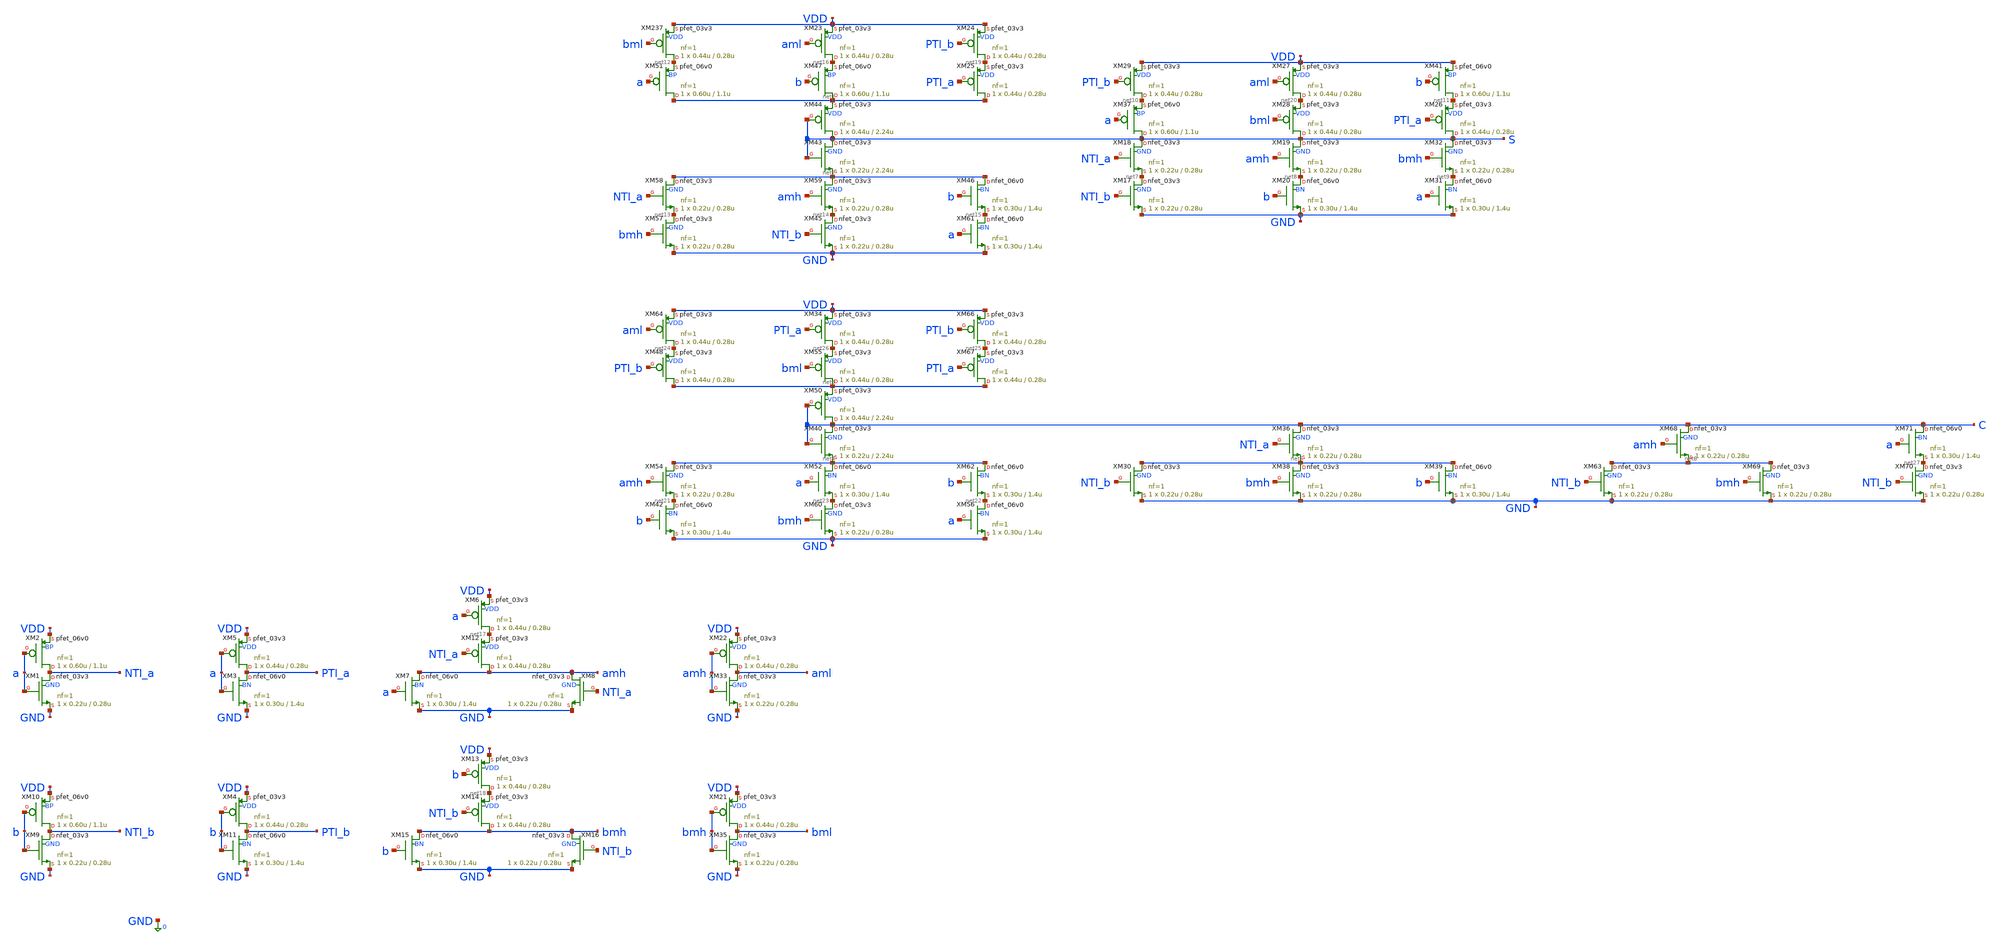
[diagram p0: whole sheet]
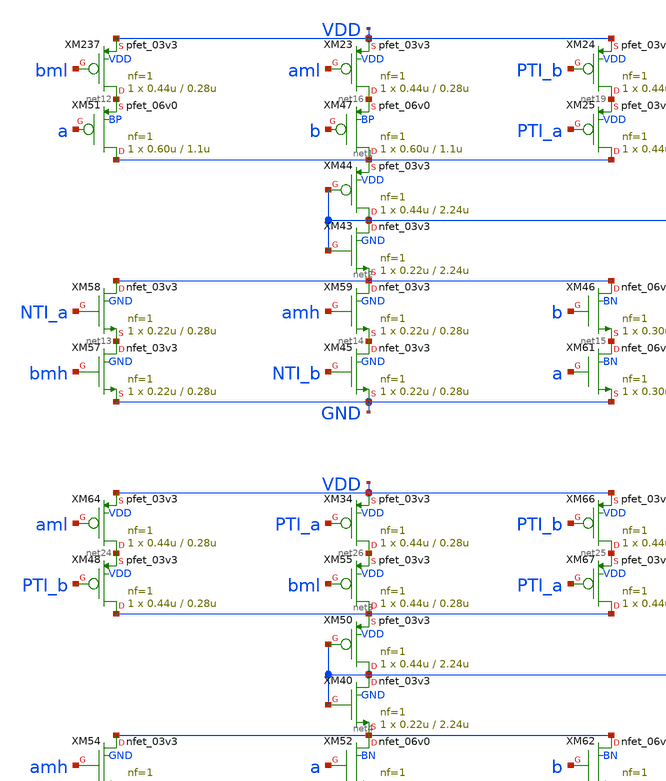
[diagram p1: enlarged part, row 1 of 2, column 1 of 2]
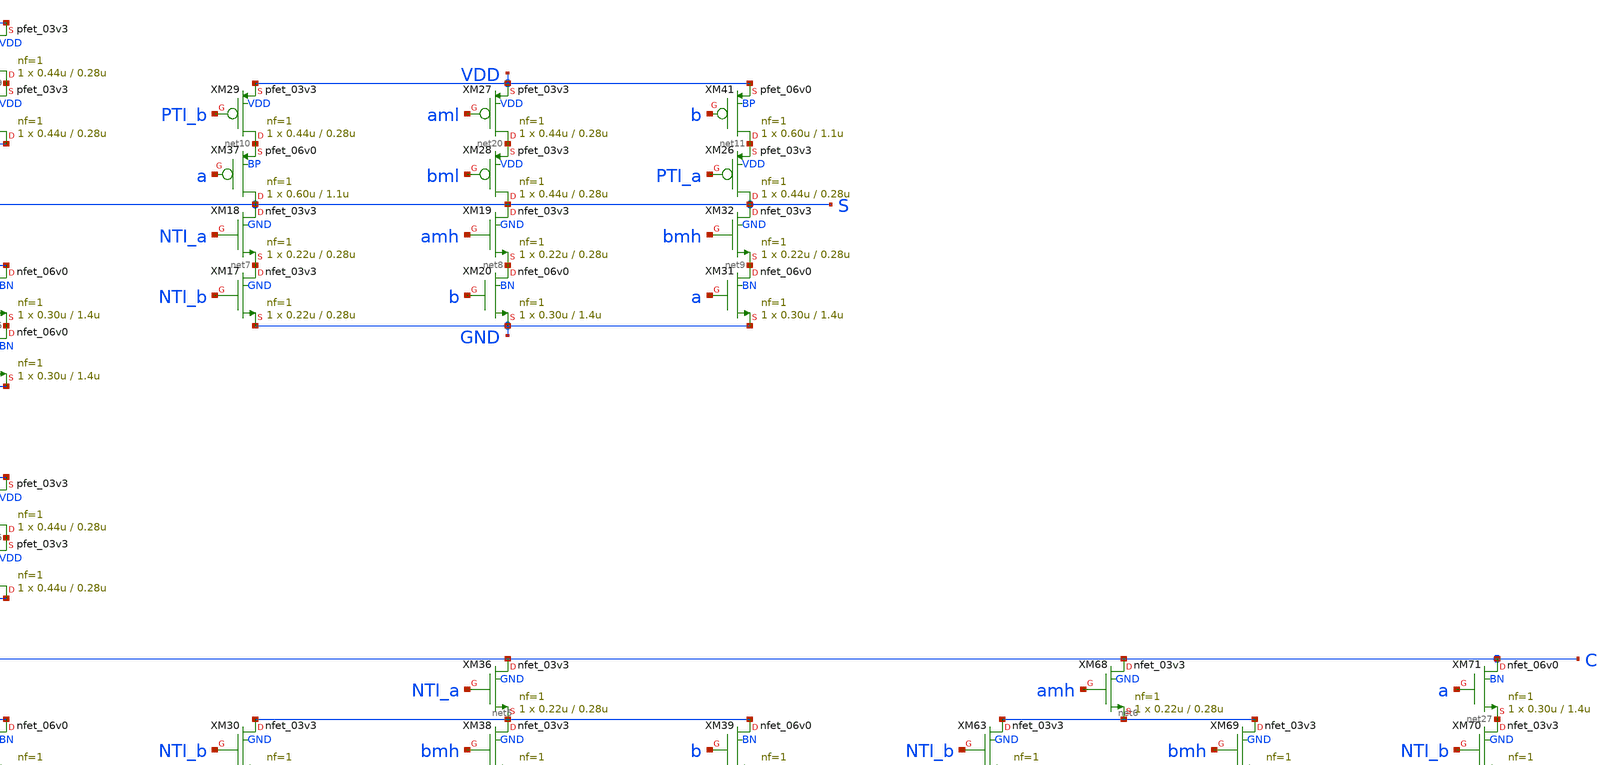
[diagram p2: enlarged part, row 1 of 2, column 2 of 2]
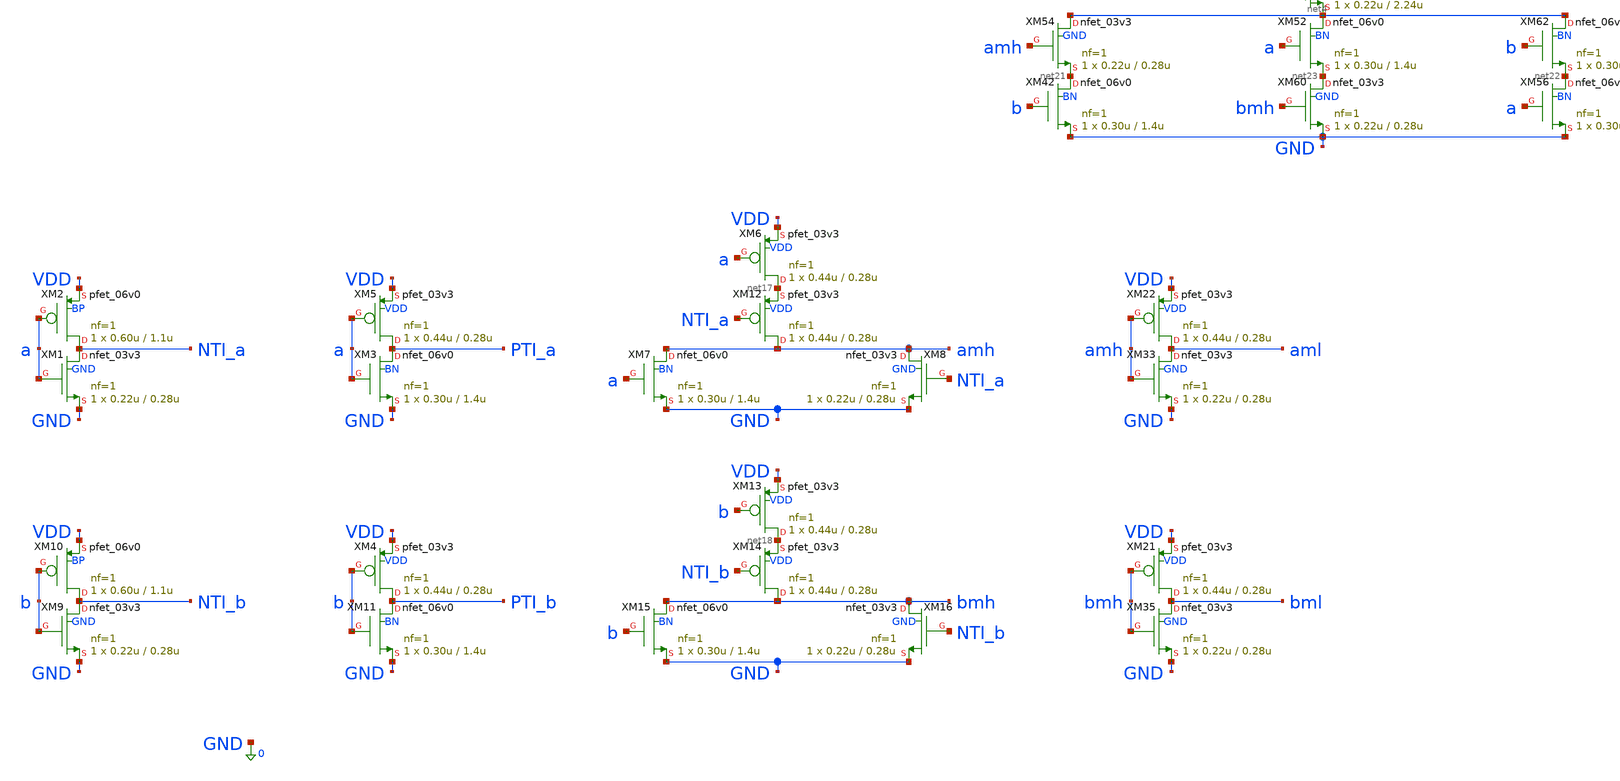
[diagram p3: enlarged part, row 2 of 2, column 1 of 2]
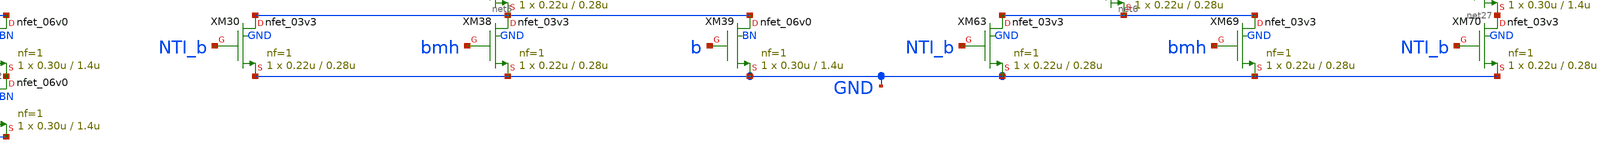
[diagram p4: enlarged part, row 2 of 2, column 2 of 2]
** sch_path: xschem_designs/SUM_TB.sch
**.subckt SUM_TB
XM1 NTI_a a GND GND nfet_03v3 L=0.28u W=0.22u nf=1 ad='int((nf+1)/2) * W/nf * 0.18u' as='int((nf+2)/2) * W/nf * 0.18u'
+ pd='2*int((nf+1)/2) * (W/nf + 0.18u)' ps='2*int((nf+2)/2) * (W/nf + 0.18u)' nrd='0.18u / W' nrs='0.18u / W'
+ sa=0 sb=0 sd=0 m=1 par=1
XM2 NTI_a a VDD BP pfet_06v0 L=1.1u W=0.60u nf=1 ad='int((nf+1)/2) * W/nf * 0.18u' as='int((nf+2)/2) * W/nf * 0.18u'
+ pd='2*int((nf+1)/2) * (W/nf + 0.18u)' ps='2*int((nf+2)/2) * (W/nf + 0.18u)' nrd='0.18u / W' nrs='0.18u / W'
+ sa=0 sb=0 sd=0 m=1 par=1
XM3 PTI_a a GND BN nfet_06v0 L=1.4u W=0.30u nf=1 ad='int((nf+1)/2) * W/nf * 0.18u' as='int((nf+2)/2) * W/nf * 0.18u'
+ pd='2*int((nf+1)/2) * (W/nf + 0.18u)' ps='2*int((nf+2)/2) * (W/nf + 0.18u)' nrd='0.18u / W' nrs='0.18u / W'
+ sa=0 sb=0 sd=0 m=1 par=1
XM7 amh a GND BN nfet_06v0 L=1.4u W=0.30u nf=1 ad='int((nf+1)/2) * W/nf * 0.18u' as='int((nf+2)/2) * W/nf * 0.18u'
+ pd='2*int((nf+1)/2) * (W/nf + 0.18u)' ps='2*int((nf+2)/2) * (W/nf + 0.18u)' nrd='0.18u / W' nrs='0.18u / W'
+ sa=0 sb=0 sd=0 m=1 par=1
XM8 amh NTI_a GND GND nfet_03v3 L=0.28u W=0.22u nf=1 ad='int((nf+1)/2) * W/nf * 0.18u' as='int((nf+2)/2) * W/nf * 0.18u'
+ pd='2*int((nf+1)/2) * (W/nf + 0.18u)' ps='2*int((nf+2)/2) * (W/nf + 0.18u)' nrd='0.18u / W' nrs='0.18u / W'
+ sa=0 sb=0 sd=0 m=1 par=1
XM9 NTI_b b GND GND nfet_03v3 L=0.28u W=0.22u nf=1 ad='int((nf+1)/2) * W/nf * 0.18u' as='int((nf+2)/2) * W/nf * 0.18u'
+ pd='2*int((nf+1)/2) * (W/nf + 0.18u)' ps='2*int((nf+2)/2) * (W/nf + 0.18u)' nrd='0.18u / W' nrs='0.18u / W'
+ sa=0 sb=0 sd=0 m=1 par=1
XM10 NTI_b b VDD BP pfet_06v0 L=1.1u W=0.60u nf=1 ad='int((nf+1)/2) * W/nf * 0.18u' as='int((nf+2)/2) * W/nf * 0.18u'
+ pd='2*int((nf+1)/2) * (W/nf + 0.18u)' ps='2*int((nf+2)/2) * (W/nf + 0.18u)' nrd='0.18u / W' nrs='0.18u / W'
+ sa=0 sb=0 sd=0 m=1 par=1
XM11 PTI_b b GND BN nfet_06v0 L=1.4u W=0.30u nf=1 ad='int((nf+1)/2) * W/nf * 0.18u' as='int((nf+2)/2) * W/nf * 0.18u'
+ pd='2*int((nf+1)/2) * (W/nf + 0.18u)' ps='2*int((nf+2)/2) * (W/nf + 0.18u)' nrd='0.18u / W' nrs='0.18u / W'
+ sa=0 sb=0 sd=0 m=1 par=1
XM15 bmh b GND BN nfet_06v0 L=1.4u W=0.30u nf=1 ad='int((nf+1)/2) * W/nf * 0.18u' as='int((nf+2)/2) * W/nf * 0.18u'
+ pd='2*int((nf+1)/2) * (W/nf + 0.18u)' ps='2*int((nf+2)/2) * (W/nf + 0.18u)' nrd='0.18u / W' nrs='0.18u / W'
+ sa=0 sb=0 sd=0 m=1 par=1
XM16 bmh NTI_b GND GND nfet_03v3 L=0.28u W=0.22u nf=1 ad='int((nf+1)/2) * W/nf * 0.18u' as='int((nf+2)/2) * W/nf * 0.18u'
+ pd='2*int((nf+1)/2) * (W/nf + 0.18u)' ps='2*int((nf+2)/2) * (W/nf + 0.18u)' nrd='0.18u / W' nrs='0.18u / W'
+ sa=0 sb=0 sd=0 m=1 par=1
XM17 net7 NTI_b GND GND nfet_03v3 L=0.28u W=0.22u nf=1 ad='int((nf+1)/2) * W/nf * 0.18u' as='int((nf+2)/2) * W/nf * 0.18u'
+ pd='2*int((nf+1)/2) * (W/nf + 0.18u)' ps='2*int((nf+2)/2) * (W/nf + 0.18u)' nrd='0.18u / W' nrs='0.18u / W'
+ sa=0 sb=0 sd=0 m=1 par=1
XM18 S NTI_a net7 GND nfet_03v3 L=0.28u W=0.22u nf=1 ad='int((nf+1)/2) * W/nf * 0.18u' as='int((nf+2)/2) * W/nf * 0.18u'
+ pd='2*int((nf+1)/2) * (W/nf + 0.18u)' ps='2*int((nf+2)/2) * (W/nf + 0.18u)' nrd='0.18u / W' nrs='0.18u / W'
+ sa=0 sb=0 sd=0 m=1 par=1
XM19 S amh net8 GND nfet_03v3 L=0.28u W=0.22u nf=1 ad='int((nf+1)/2) * W/nf * 0.18u' as='int((nf+2)/2) * W/nf * 0.18u'
+ pd='2*int((nf+1)/2) * (W/nf + 0.18u)' ps='2*int((nf+2)/2) * (W/nf + 0.18u)' nrd='0.18u / W' nrs='0.18u / W'
+ sa=0 sb=0 sd=0 m=1 par=1
XM20 net8 b GND BN nfet_06v0 L=1.4u W=0.30u nf=1 ad='int((nf+1)/2) * W/nf * 0.18u' as='int((nf+2)/2) * W/nf * 0.18u'
+ pd='2*int((nf+1)/2) * (W/nf + 0.18u)' ps='2*int((nf+2)/2) * (W/nf + 0.18u)' nrd='0.18u / W' nrs='0.18u / W'
+ sa=0 sb=0 sd=0 m=1 par=1
XM31 net9 a GND BN nfet_06v0 L=1.4u W=0.30u nf=1 ad='int((nf+1)/2) * W/nf * 0.18u' as='int((nf+2)/2) * W/nf * 0.18u'
+ pd='2*int((nf+1)/2) * (W/nf + 0.18u)' ps='2*int((nf+2)/2) * (W/nf + 0.18u)' nrd='0.18u / W' nrs='0.18u / W'
+ sa=0 sb=0 sd=0 m=1 par=1
XM32 S bmh net9 GND nfet_03v3 L=0.28u W=0.22u nf=1 ad='int((nf+1)/2) * W/nf * 0.18u' as='int((nf+2)/2) * W/nf * 0.18u'
+ pd='2*int((nf+1)/2) * (W/nf + 0.18u)' ps='2*int((nf+2)/2) * (W/nf + 0.18u)' nrd='0.18u / W' nrs='0.18u / W'
+ sa=0 sb=0 sd=0 m=1 par=1
XM33 aml amh GND GND nfet_03v3 L=0.28u W=0.22u nf=1 ad='int((nf+1)/2) * W/nf * 0.18u' as='int((nf+2)/2) * W/nf * 0.18u'
+ pd='2*int((nf+1)/2) * (W/nf + 0.18u)' ps='2*int((nf+2)/2) * (W/nf + 0.18u)' nrd='0.18u / W' nrs='0.18u / W'
+ sa=0 sb=0 sd=0 m=1 par=1
XM35 bml bmh GND GND nfet_03v3 L=0.28u W=0.22u nf=1 ad='int((nf+1)/2) * W/nf * 0.18u' as='int((nf+2)/2) * W/nf * 0.18u'
+ pd='2*int((nf+1)/2) * (W/nf + 0.18u)' ps='2*int((nf+2)/2) * (W/nf + 0.18u)' nrd='0.18u / W' nrs='0.18u / W'
+ sa=0 sb=0 sd=0 m=1 par=1
XM37 S a net10 BP pfet_06v0 L=1.1u W=0.60u nf=1 ad='int((nf+1)/2) * W/nf * 0.18u' as='int((nf+2)/2) * W/nf * 0.18u'
+ pd='2*int((nf+1)/2) * (W/nf + 0.18u)' ps='2*int((nf+2)/2) * (W/nf + 0.18u)' nrd='0.18u / W' nrs='0.18u / W'
+ sa=0 sb=0 sd=0 m=1 par=1
XM41 net11 b VDD BP pfet_06v0 L=1.1u W=0.60u nf=1 ad='int((nf+1)/2) * W/nf * 0.18u' as='int((nf+2)/2) * W/nf * 0.18u'
+ pd='2*int((nf+1)/2) * (W/nf + 0.18u)' ps='2*int((nf+2)/2) * (W/nf + 0.18u)' nrd='0.18u / W' nrs='0.18u / W'
+ sa=0 sb=0 sd=0 m=1 par=1
XM43 S S net2 GND nfet_03v3 L=2.24u W=0.22u nf=1 ad='int((nf+1)/2) * W/nf * 0.18u' as='int((nf+2)/2) * W/nf * 0.18u'
+ pd='2*int((nf+1)/2) * (W/nf + 0.18u)' ps='2*int((nf+2)/2) * (W/nf + 0.18u)' nrd='0.18u / W' nrs='0.18u / W'
+ sa=0 sb=0 sd=0 m=1 par=1
XM44 S S net1 VDD pfet_03v3 L=2.24u W=0.44u nf=1 ad='int((nf+1)/2) * W/nf * 0.18u' as='int((nf+2)/2) * W/nf * 0.18u'
+ pd='2*int((nf+1)/2) * (W/nf + 0.18u)' ps='2*int((nf+2)/2) * (W/nf + 0.18u)' nrd='0.18u / W' nrs='0.18u / W'
+ sa=0 sb=0 sd=0 m=1 par=1
XM51 net1 a net12 BP pfet_06v0 L=1.1u W=0.60u nf=1 ad='int((nf+1)/2) * W/nf * 0.18u' as='int((nf+2)/2) * W/nf * 0.18u'
+ pd='2*int((nf+1)/2) * (W/nf + 0.18u)' ps='2*int((nf+2)/2) * (W/nf + 0.18u)' nrd='0.18u / W' nrs='0.18u / W'
+ sa=0 sb=0 sd=0 m=1 par=1
XM57 net13 bmh GND GND nfet_03v3 L=0.28u W=0.22u nf=1 ad='int((nf+1)/2) * W/nf * 0.18u' as='int((nf+2)/2) * W/nf * 0.18u'
+ pd='2*int((nf+1)/2) * (W/nf + 0.18u)' ps='2*int((nf+2)/2) * (W/nf + 0.18u)' nrd='0.18u / W' nrs='0.18u / W'
+ sa=0 sb=0 sd=0 m=1 par=1
XM58 net2 NTI_a net13 GND nfet_03v3 L=0.28u W=0.22u nf=1 ad='int((nf+1)/2) * W/nf * 0.18u' as='int((nf+2)/2) * W/nf * 0.18u'
+ pd='2*int((nf+1)/2) * (W/nf + 0.18u)' ps='2*int((nf+2)/2) * (W/nf + 0.18u)' nrd='0.18u / W' nrs='0.18u / W'
+ sa=0 sb=0 sd=0 m=1 par=1
XM59 net2 amh net14 GND nfet_03v3 L=0.28u W=0.22u nf=1 ad='int((nf+1)/2) * W/nf * 0.18u' as='int((nf+2)/2) * W/nf * 0.18u'
+ pd='2*int((nf+1)/2) * (W/nf + 0.18u)' ps='2*int((nf+2)/2) * (W/nf + 0.18u)' nrd='0.18u / W' nrs='0.18u / W'
+ sa=0 sb=0 sd=0 m=1 par=1
XM61 net15 a GND BN nfet_06v0 L=1.4u W=0.30u nf=1 ad='int((nf+1)/2) * W/nf * 0.18u' as='int((nf+2)/2) * W/nf * 0.18u'
+ pd='2*int((nf+1)/2) * (W/nf + 0.18u)' ps='2*int((nf+2)/2) * (W/nf + 0.18u)' nrd='0.18u / W' nrs='0.18u / W'
+ sa=0 sb=0 sd=0 m=1 par=1
XM45 net14 NTI_b GND GND nfet_03v3 L=0.28u W=0.22u nf=1 ad='int((nf+1)/2) * W/nf * 0.18u' as='int((nf+2)/2) * W/nf * 0.18u'
+ pd='2*int((nf+1)/2) * (W/nf + 0.18u)' ps='2*int((nf+2)/2) * (W/nf + 0.18u)' nrd='0.18u / W' nrs='0.18u / W'
+ sa=0 sb=0 sd=0 m=1 par=1
XM46 net2 b net15 BN nfet_06v0 L=1.4u W=0.30u nf=1 ad='int((nf+1)/2) * W/nf * 0.18u' as='int((nf+2)/2) * W/nf * 0.18u'
+ pd='2*int((nf+1)/2) * (W/nf + 0.18u)' ps='2*int((nf+2)/2) * (W/nf + 0.18u)' nrd='0.18u / W' nrs='0.18u / W'
+ sa=0 sb=0 sd=0 m=1 par=1
XM47 net1 b net16 BP pfet_06v0 L=1.1u W=0.60u nf=1 ad='int((nf+1)/2) * W/nf * 0.18u' as='int((nf+2)/2) * W/nf * 0.18u'
+ pd='2*int((nf+1)/2) * (W/nf + 0.18u)' ps='2*int((nf+2)/2) * (W/nf + 0.18u)' nrd='0.18u / W' nrs='0.18u / W'
+ sa=0 sb=0 sd=0 m=1 par=1
XM237 net12 bml VDD VDD pfet_03v3 L=0.28u W=0.44u nf=1 ad='int((nf+1)/2) * W/nf * 0.18u' as='int((nf+2)/2) * W/nf * 0.18u'
+ pd='2*int((nf+1)/2) * (W/nf + 0.18u)' ps='2*int((nf+2)/2) * (W/nf + 0.18u)' nrd='0.18u / W' nrs='0.18u / W'
+ sa=0 sb=0 sd=0 m=1 par=1
XM4 PTI_b b VDD VDD pfet_03v3 L=0.28u W=0.44u nf=1 ad='int((nf+1)/2) * W/nf * 0.18u' as='int((nf+2)/2) * W/nf * 0.18u'
+ pd='2*int((nf+1)/2) * (W/nf + 0.18u)' ps='2*int((nf+2)/2) * (W/nf + 0.18u)' nrd='0.18u / W' nrs='0.18u / W'
+ sa=0 sb=0 sd=0 m=1 par=1
XM5 PTI_a a VDD VDD pfet_03v3 L=0.28u W=0.44u nf=1 ad='int((nf+1)/2) * W/nf * 0.18u' as='int((nf+2)/2) * W/nf * 0.18u'
+ pd='2*int((nf+1)/2) * (W/nf + 0.18u)' ps='2*int((nf+2)/2) * (W/nf + 0.18u)' nrd='0.18u / W' nrs='0.18u / W'
+ sa=0 sb=0 sd=0 m=1 par=1
XM6 net17 a VDD VDD pfet_03v3 L=0.28u W=0.44u nf=1 ad='int((nf+1)/2) * W/nf * 0.18u' as='int((nf+2)/2) * W/nf * 0.18u'
+ pd='2*int((nf+1)/2) * (W/nf + 0.18u)' ps='2*int((nf+2)/2) * (W/nf + 0.18u)' nrd='0.18u / W' nrs='0.18u / W'
+ sa=0 sb=0 sd=0 m=1 par=1
XM12 amh NTI_a net17 VDD pfet_03v3 L=0.28u W=0.44u nf=1 ad='int((nf+1)/2) * W/nf * 0.18u' as='int((nf+2)/2) * W/nf * 0.18u'
+ pd='2*int((nf+1)/2) * (W/nf + 0.18u)' ps='2*int((nf+2)/2) * (W/nf + 0.18u)' nrd='0.18u / W' nrs='0.18u / W'
+ sa=0 sb=0 sd=0 m=1 par=1
XM13 net18 b VDD VDD pfet_03v3 L=0.28u W=0.44u nf=1 ad='int((nf+1)/2) * W/nf * 0.18u' as='int((nf+2)/2) * W/nf * 0.18u'
+ pd='2*int((nf+1)/2) * (W/nf + 0.18u)' ps='2*int((nf+2)/2) * (W/nf + 0.18u)' nrd='0.18u / W' nrs='0.18u / W'
+ sa=0 sb=0 sd=0 m=1 par=1
XM14 bmh NTI_b net18 VDD pfet_03v3 L=0.28u W=0.44u nf=1 ad='int((nf+1)/2) * W/nf * 0.18u' as='int((nf+2)/2) * W/nf * 0.18u'
+ pd='2*int((nf+1)/2) * (W/nf + 0.18u)' ps='2*int((nf+2)/2) * (W/nf + 0.18u)' nrd='0.18u / W' nrs='0.18u / W'
+ sa=0 sb=0 sd=0 m=1 par=1
XM21 bml bmh VDD VDD pfet_03v3 L=0.28u W=0.44u nf=1 ad='int((nf+1)/2) * W/nf * 0.18u' as='int((nf+2)/2) * W/nf * 0.18u'
+ pd='2*int((nf+1)/2) * (W/nf + 0.18u)' ps='2*int((nf+2)/2) * (W/nf + 0.18u)' nrd='0.18u / W' nrs='0.18u / W'
+ sa=0 sb=0 sd=0 m=1 par=1
XM22 aml amh VDD VDD pfet_03v3 L=0.28u W=0.44u nf=1 ad='int((nf+1)/2) * W/nf * 0.18u' as='int((nf+2)/2) * W/nf * 0.18u'
+ pd='2*int((nf+1)/2) * (W/nf + 0.18u)' ps='2*int((nf+2)/2) * (W/nf + 0.18u)' nrd='0.18u / W' nrs='0.18u / W'
+ sa=0 sb=0 sd=0 m=1 par=1
XM23 net16 aml VDD VDD pfet_03v3 L=0.28u W=0.44u nf=1 ad='int((nf+1)/2) * W/nf * 0.18u' as='int((nf+2)/2) * W/nf * 0.18u'
+ pd='2*int((nf+1)/2) * (W/nf + 0.18u)' ps='2*int((nf+2)/2) * (W/nf + 0.18u)' nrd='0.18u / W' nrs='0.18u / W'
+ sa=0 sb=0 sd=0 m=1 par=1
XM24 net19 PTI_b VDD VDD pfet_03v3 L=0.28u W=0.44u nf=1 ad='int((nf+1)/2) * W/nf * 0.18u' as='int((nf+2)/2) * W/nf * 0.18u'
+ pd='2*int((nf+1)/2) * (W/nf + 0.18u)' ps='2*int((nf+2)/2) * (W/nf + 0.18u)' nrd='0.18u / W' nrs='0.18u / W'
+ sa=0 sb=0 sd=0 m=1 par=1
XM25 net1 PTI_a net19 VDD pfet_03v3 L=0.28u W=0.44u nf=1 ad='int((nf+1)/2) * W/nf * 0.18u' as='int((nf+2)/2) * W/nf * 0.18u'
+ pd='2*int((nf+1)/2) * (W/nf + 0.18u)' ps='2*int((nf+2)/2) * (W/nf + 0.18u)' nrd='0.18u / W' nrs='0.18u / W'
+ sa=0 sb=0 sd=0 m=1 par=1
XM26 S PTI_a net11 VDD pfet_03v3 L=0.28u W=0.44u nf=1 ad='int((nf+1)/2) * W/nf * 0.18u' as='int((nf+2)/2) * W/nf * 0.18u'
+ pd='2*int((nf+1)/2) * (W/nf + 0.18u)' ps='2*int((nf+2)/2) * (W/nf + 0.18u)' nrd='0.18u / W' nrs='0.18u / W'
+ sa=0 sb=0 sd=0 m=1 par=1
XM27 net20 aml VDD VDD pfet_03v3 L=0.28u W=0.44u nf=1 ad='int((nf+1)/2) * W/nf * 0.18u' as='int((nf+2)/2) * W/nf * 0.18u'
+ pd='2*int((nf+1)/2) * (W/nf + 0.18u)' ps='2*int((nf+2)/2) * (W/nf + 0.18u)' nrd='0.18u / W' nrs='0.18u / W'
+ sa=0 sb=0 sd=0 m=1 par=1
XM28 S bml net20 VDD pfet_03v3 L=0.28u W=0.44u nf=1 ad='int((nf+1)/2) * W/nf * 0.18u' as='int((nf+2)/2) * W/nf * 0.18u'
+ pd='2*int((nf+1)/2) * (W/nf + 0.18u)' ps='2*int((nf+2)/2) * (W/nf + 0.18u)' nrd='0.18u / W' nrs='0.18u / W'
+ sa=0 sb=0 sd=0 m=1 par=1
XM29 net10 PTI_b VDD VDD pfet_03v3 L=0.28u W=0.44u nf=1 ad='int((nf+1)/2) * W/nf * 0.18u' as='int((nf+2)/2) * W/nf * 0.18u'
+ pd='2*int((nf+1)/2) * (W/nf + 0.18u)' ps='2*int((nf+2)/2) * (W/nf + 0.18u)' nrd='0.18u / W' nrs='0.18u / W'
+ sa=0 sb=0 sd=0 m=1 par=1
XM30 net5 NTI_b GND GND nfet_03v3 L=0.28u W=0.22u nf=1 ad='int((nf+1)/2) * W/nf * 0.18u' as='int((nf+2)/2) * W/nf * 0.18u'
+ pd='2*int((nf+1)/2) * (W/nf + 0.18u)' ps='2*int((nf+2)/2) * (W/nf + 0.18u)' nrd='0.18u / W' nrs='0.18u / W'
+ sa=0 sb=0 sd=0 m=1 par=1
XM36 C NTI_a net5 GND nfet_03v3 L=0.28u W=0.22u nf=1 ad='int((nf+1)/2) * W/nf * 0.18u' as='int((nf+2)/2) * W/nf * 0.18u'
+ pd='2*int((nf+1)/2) * (W/nf + 0.18u)' ps='2*int((nf+2)/2) * (W/nf + 0.18u)' nrd='0.18u / W' nrs='0.18u / W'
+ sa=0 sb=0 sd=0 m=1 par=1
XM39 net5 b GND BN nfet_06v0 L=1.4u W=0.30u nf=1 ad='int((nf+1)/2) * W/nf * 0.18u' as='int((nf+2)/2) * W/nf * 0.18u'
+ pd='2*int((nf+1)/2) * (W/nf + 0.18u)' ps='2*int((nf+2)/2) * (W/nf + 0.18u)' nrd='0.18u / W' nrs='0.18u / W'
+ sa=0 sb=0 sd=0 m=1 par=1
XM50 C C net3 VDD pfet_03v3 L=2.24u W=0.44u nf=1 ad='int((nf+1)/2) * W/nf * 0.18u' as='int((nf+2)/2) * W/nf * 0.18u'
+ pd='2*int((nf+1)/2) * (W/nf + 0.18u)' ps='2*int((nf+2)/2) * (W/nf + 0.18u)' nrd='0.18u / W' nrs='0.18u / W'
+ sa=0 sb=0 sd=0 m=1 par=1
XM54 net4 amh net21 GND nfet_03v3 L=0.28u W=0.22u nf=1 ad='int((nf+1)/2) * W/nf * 0.18u' as='int((nf+2)/2) * W/nf * 0.18u'
+ pd='2*int((nf+1)/2) * (W/nf + 0.18u)' ps='2*int((nf+2)/2) * (W/nf + 0.18u)' nrd='0.18u / W' nrs='0.18u / W'
+ sa=0 sb=0 sd=0 m=1 par=1
XM56 net22 a GND BN nfet_06v0 L=1.4u W=0.30u nf=1 ad='int((nf+1)/2) * W/nf * 0.18u' as='int((nf+2)/2) * W/nf * 0.18u'
+ pd='2*int((nf+1)/2) * (W/nf + 0.18u)' ps='2*int((nf+2)/2) * (W/nf + 0.18u)' nrd='0.18u / W' nrs='0.18u / W'
+ sa=0 sb=0 sd=0 m=1 par=1
XM60 net23 bmh GND GND nfet_03v3 L=0.28u W=0.22u nf=1 ad='int((nf+1)/2) * W/nf * 0.18u' as='int((nf+2)/2) * W/nf * 0.18u'
+ pd='2*int((nf+1)/2) * (W/nf + 0.18u)' ps='2*int((nf+2)/2) * (W/nf + 0.18u)' nrd='0.18u / W' nrs='0.18u / W'
+ sa=0 sb=0 sd=0 m=1 par=1
XM62 net4 b net22 BN nfet_06v0 L=1.4u W=0.30u nf=1 ad='int((nf+1)/2) * W/nf * 0.18u' as='int((nf+2)/2) * W/nf * 0.18u'
+ pd='2*int((nf+1)/2) * (W/nf + 0.18u)' ps='2*int((nf+2)/2) * (W/nf + 0.18u)' nrd='0.18u / W' nrs='0.18u / W'
+ sa=0 sb=0 sd=0 m=1 par=1
XM64 net24 aml VDD VDD pfet_03v3 L=0.28u W=0.44u nf=1 ad='int((nf+1)/2) * W/nf * 0.18u' as='int((nf+2)/2) * W/nf * 0.18u'
+ pd='2*int((nf+1)/2) * (W/nf + 0.18u)' ps='2*int((nf+2)/2) * (W/nf + 0.18u)' nrd='0.18u / W' nrs='0.18u / W'
+ sa=0 sb=0 sd=0 m=1 par=1
XM66 net25 PTI_b VDD VDD pfet_03v3 L=0.28u W=0.44u nf=1 ad='int((nf+1)/2) * W/nf * 0.18u' as='int((nf+2)/2) * W/nf * 0.18u'
+ pd='2*int((nf+1)/2) * (W/nf + 0.18u)' ps='2*int((nf+2)/2) * (W/nf + 0.18u)' nrd='0.18u / W' nrs='0.18u / W'
+ sa=0 sb=0 sd=0 m=1 par=1
XM67 net3 PTI_a net25 VDD pfet_03v3 L=0.28u W=0.44u nf=1 ad='int((nf+1)/2) * W/nf * 0.18u' as='int((nf+2)/2) * W/nf * 0.18u'
+ pd='2*int((nf+1)/2) * (W/nf + 0.18u)' ps='2*int((nf+2)/2) * (W/nf + 0.18u)' nrd='0.18u / W' nrs='0.18u / W'
+ sa=0 sb=0 sd=0 m=1 par=1
XM42 net21 b GND BN nfet_06v0 L=1.4u W=0.30u nf=1 ad='int((nf+1)/2) * W/nf * 0.18u' as='int((nf+2)/2) * W/nf * 0.18u'
+ pd='2*int((nf+1)/2) * (W/nf + 0.18u)' ps='2*int((nf+2)/2) * (W/nf + 0.18u)' nrd='0.18u / W' nrs='0.18u / W'
+ sa=0 sb=0 sd=0 m=1 par=1
XM48 net3 PTI_b net24 VDD pfet_03v3 L=0.28u W=0.44u nf=1 ad='int((nf+1)/2) * W/nf * 0.18u' as='int((nf+2)/2) * W/nf * 0.18u'
+ pd='2*int((nf+1)/2) * (W/nf + 0.18u)' ps='2*int((nf+2)/2) * (W/nf + 0.18u)' nrd='0.18u / W' nrs='0.18u / W'
+ sa=0 sb=0 sd=0 m=1 par=1
XM52 net4 a net23 BN nfet_06v0 L=1.4u W=0.30u nf=1 ad='int((nf+1)/2) * W/nf * 0.18u' as='int((nf+2)/2) * W/nf * 0.18u'
+ pd='2*int((nf+1)/2) * (W/nf + 0.18u)' ps='2*int((nf+2)/2) * (W/nf + 0.18u)' nrd='0.18u / W' nrs='0.18u / W'
+ sa=0 sb=0 sd=0 m=1 par=1
XM55 net3 bml net26 VDD pfet_03v3 L=0.28u W=0.44u nf=1 ad='int((nf+1)/2) * W/nf * 0.18u' as='int((nf+2)/2) * W/nf * 0.18u'
+ pd='2*int((nf+1)/2) * (W/nf + 0.18u)' ps='2*int((nf+2)/2) * (W/nf + 0.18u)' nrd='0.18u / W' nrs='0.18u / W'
+ sa=0 sb=0 sd=0 m=1 par=1
XM63 net6 NTI_b GND GND nfet_03v3 L=0.28u W=0.22u nf=1 ad='int((nf+1)/2) * W/nf * 0.18u' as='int((nf+2)/2) * W/nf * 0.18u'
+ pd='2*int((nf+1)/2) * (W/nf + 0.18u)' ps='2*int((nf+2)/2) * (W/nf + 0.18u)' nrd='0.18u / W' nrs='0.18u / W'
+ sa=0 sb=0 sd=0 m=1 par=1
XM68 C amh net6 GND nfet_03v3 L=0.28u W=0.22u nf=1 ad='int((nf+1)/2) * W/nf * 0.18u' as='int((nf+2)/2) * W/nf * 0.18u'
+ pd='2*int((nf+1)/2) * (W/nf + 0.18u)' ps='2*int((nf+2)/2) * (W/nf + 0.18u)' nrd='0.18u / W' nrs='0.18u / W'
+ sa=0 sb=0 sd=0 m=1 par=1
XM38 net5 bmh GND GND nfet_03v3 L=0.28u W=0.22u nf=1 ad='int((nf+1)/2) * W/nf * 0.18u' as='int((nf+2)/2) * W/nf * 0.18u'
+ pd='2*int((nf+1)/2) * (W/nf + 0.18u)' ps='2*int((nf+2)/2) * (W/nf + 0.18u)' nrd='0.18u / W' nrs='0.18u / W'
+ sa=0 sb=0 sd=0 m=1 par=1
XM69 net6 bmh GND GND nfet_03v3 L=0.28u W=0.22u nf=1 ad='int((nf+1)/2) * W/nf * 0.18u' as='int((nf+2)/2) * W/nf * 0.18u'
+ pd='2*int((nf+1)/2) * (W/nf + 0.18u)' ps='2*int((nf+2)/2) * (W/nf + 0.18u)' nrd='0.18u / W' nrs='0.18u / W'
+ sa=0 sb=0 sd=0 m=1 par=1
XM70 net27 NTI_b GND GND nfet_03v3 L=0.28u W=0.22u nf=1 ad='int((nf+1)/2) * W/nf * 0.18u' as='int((nf+2)/2) * W/nf * 0.18u'
+ pd='2*int((nf+1)/2) * (W/nf + 0.18u)' ps='2*int((nf+2)/2) * (W/nf + 0.18u)' nrd='0.18u / W' nrs='0.18u / W'
+ sa=0 sb=0 sd=0 m=1 par=1
XM71 C a net27 BN nfet_06v0 L=1.4u W=0.30u nf=1 ad='int((nf+1)/2) * W/nf * 0.18u' as='int((nf+2)/2) * W/nf * 0.18u'
+ pd='2*int((nf+1)/2) * (W/nf + 0.18u)' ps='2*int((nf+2)/2) * (W/nf + 0.18u)' nrd='0.18u / W' nrs='0.18u / W'
+ sa=0 sb=0 sd=0 m=1 par=1
XM34 net26 PTI_a VDD VDD pfet_03v3 L=0.28u W=0.44u nf=1 ad='int((nf+1)/2) * W/nf * 0.18u' as='int((nf+2)/2) * W/nf * 0.18u'
+ pd='2*int((nf+1)/2) * (W/nf + 0.18u)' ps='2*int((nf+2)/2) * (W/nf + 0.18u)' nrd='0.18u / W' nrs='0.18u / W'
+ sa=0 sb=0 sd=0 m=1 par=1
XM40 C C net4 GND nfet_03v3 L=2.24u W=0.22u nf=1 ad='int((nf+1)/2) * W/nf * 0.18u' as='int((nf+2)/2) * W/nf * 0.18u'
+ pd='2*int((nf+1)/2) * (W/nf + 0.18u)' ps='2*int((nf+2)/2) * (W/nf + 0.18u)' nrd='0.18u / W' nrs='0.18u / W'
+ sa=0 sb=0 sd=0 m=1 par=1
**** begin user architecture code


.global VDD GND BP BN
.option temp=27
.include /usr/local/share/pdk/gf180mcuC/libs.tech/ngspice/design.ngspice
.lib /usr/local/share/pdk/gf180mcuC/libs.tech/ngspice/sm141064.ngspice typical

Vdd VDD 0 3.3
Vbp BP VDD 2.7
Vbn BN GND -2.7
Va a 0 PWL(0 0 89.9n 0 90.1n 1.4 179.9n 1.4 180.1n 3.3 269.9n 3.3 r=0)
Vb b 0 PWL(0 0 269.9n 0 270.1n 1.4 539.9n 1.4 540.1n 3.3  809.9n 3.3 r=0)

.control
  save all
  tran 0.1n 810n
  write SUM_TB.raw
.endc
.end


**** end user architecture code
**.ends
.end
